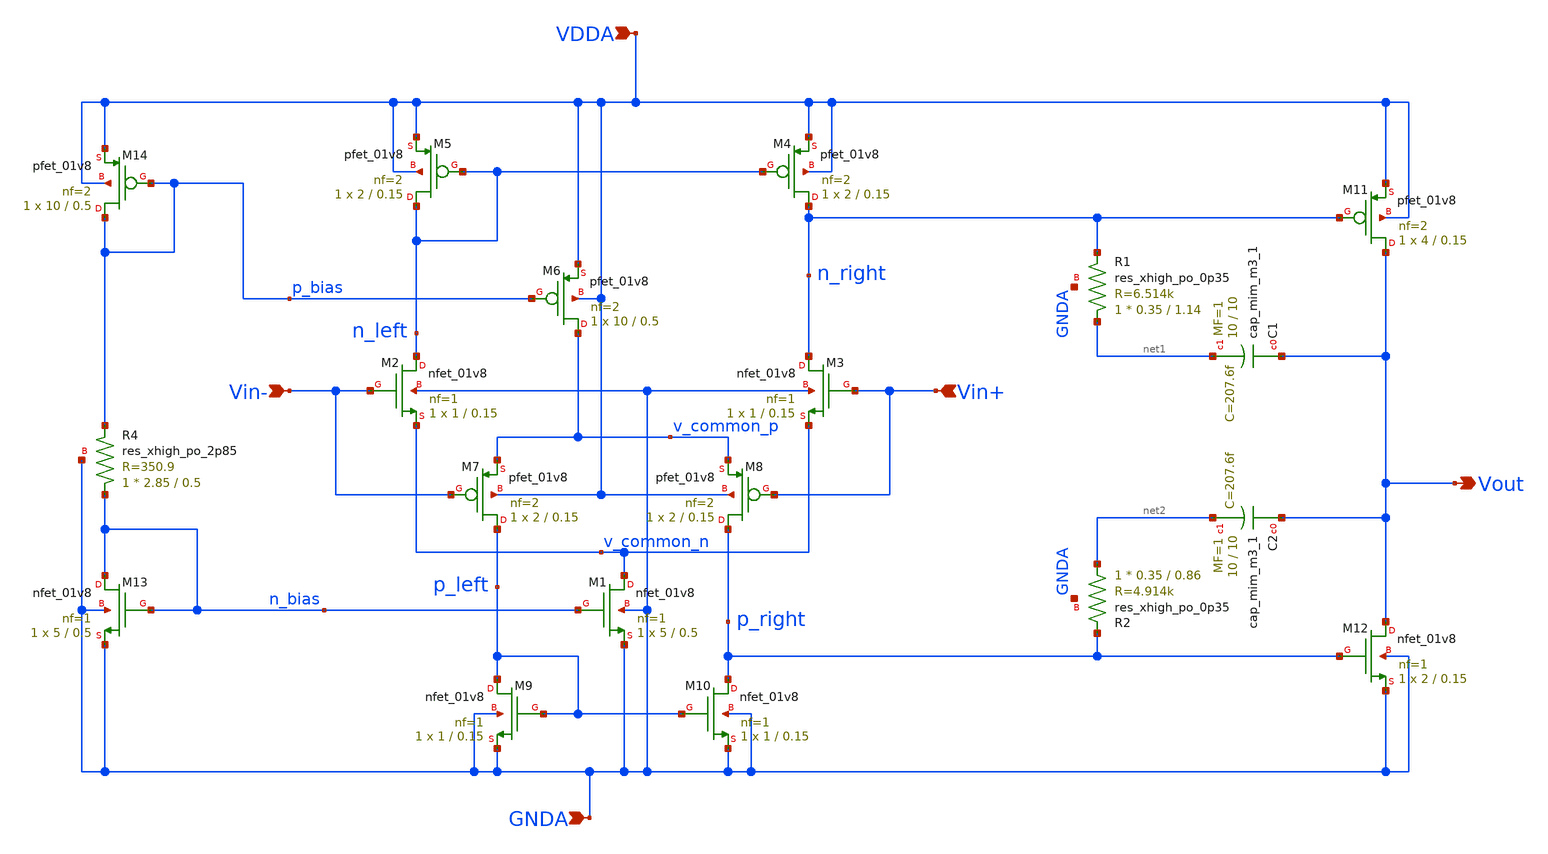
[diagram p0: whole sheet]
** sch_path: projects/pll/charge_pump/xschem_ngspice/rail_to_rail_opamp6_2.sch
**.subckt rail_to_rail_opamp6_2 Vout Vin+ Vin- VDDA GNDA
*.opin Vout
*.ipin Vin+
*.ipin Vin-
*.ipin VDDA
*.ipin GNDA
XM2 n_left Vin- v_common_n GNDA sky130_fd_pr__nfet_01v8 L=0.15 W=1 nf=1 ad='int((nf+1)/2) * W/nf * 0.29'
+ as='int((nf+2)/2) * W/nf * 0.29' pd='2*int((nf+1)/2) * (W/nf + 0.29)' ps='2*int((nf+2)/2) * (W/nf + 0.29)'
+ nrd='0.29 / W' nrs='0.29 / W' sa=0 sb=0 sd=0 mult=1 m=1
XM3 n_right Vin+ v_common_n GNDA sky130_fd_pr__nfet_01v8 L=0.15 W=1 nf=1 ad='int((nf+1)/2) * W/nf * 0.29'
+ as='int((nf+2)/2) * W/nf * 0.29' pd='2*int((nf+1)/2) * (W/nf + 0.29)' ps='2*int((nf+2)/2) * (W/nf + 0.29)'
+ nrd='0.29 / W' nrs='0.29 / W' sa=0 sb=0 sd=0 mult=1 m=1
XM5 n_left n_left VDDA VDDA sky130_fd_pr__pfet_01v8 L=0.15 W=2 nf=2 ad='int((nf+1)/2) * W/nf * 0.29'
+ as='int((nf+2)/2) * W/nf * 0.29' pd='2*int((nf+1)/2) * (W/nf + 0.29)' ps='2*int((nf+2)/2) * (W/nf + 0.29)'
+ nrd='0.29 / W' nrs='0.29 / W' sa=0 sb=0 sd=0 mult=1 m=1
XM4 n_right n_left VDDA VDDA sky130_fd_pr__pfet_01v8 L=0.15 W=2 nf=2 ad='int((nf+1)/2) * W/nf * 0.29'
+ as='int((nf+2)/2) * W/nf * 0.29' pd='2*int((nf+1)/2) * (W/nf + 0.29)' ps='2*int((nf+2)/2) * (W/nf + 0.29)'
+ nrd='0.29 / W' nrs='0.29 / W' sa=0 sb=0 sd=0 mult=1 m=1
XM6 v_common_p p_bias VDDA VDDA sky130_fd_pr__pfet_01v8 L=0.5 W=10 nf=2 ad='int((nf+1)/2) * W/nf * 0.29'
+ as='int((nf+2)/2) * W/nf * 0.29' pd='2*int((nf+1)/2) * (W/nf + 0.29)' ps='2*int((nf+2)/2) * (W/nf + 0.29)'
+ nrd='0.29 / W' nrs='0.29 / W' sa=0 sb=0 sd=0 mult=1 m=1
XM7 p_left Vin- v_common_p VDDA sky130_fd_pr__pfet_01v8 L=0.15 W=2 nf=2 ad='int((nf+1)/2) * W/nf * 0.29'
+ as='int((nf+2)/2) * W/nf * 0.29' pd='2*int((nf+1)/2) * (W/nf + 0.29)' ps='2*int((nf+2)/2) * (W/nf + 0.29)'
+ nrd='0.29 / W' nrs='0.29 / W' sa=0 sb=0 sd=0 mult=1 m=1
XM8 p_right Vin+ v_common_p VDDA sky130_fd_pr__pfet_01v8 L=0.15 W=2 nf=2 ad='int((nf+1)/2) * W/nf * 0.29'
+ as='int((nf+2)/2) * W/nf * 0.29' pd='2*int((nf+1)/2) * (W/nf + 0.29)' ps='2*int((nf+2)/2) * (W/nf + 0.29)'
+ nrd='0.29 / W' nrs='0.29 / W' sa=0 sb=0 sd=0 mult=1 m=1
XM9 p_left p_left GNDA GNDA sky130_fd_pr__nfet_01v8 L=0.15 W=1 nf=1 ad='int((nf+1)/2) * W/nf * 0.29'
+ as='int((nf+2)/2) * W/nf * 0.29' pd='2*int((nf+1)/2) * (W/nf + 0.29)' ps='2*int((nf+2)/2) * (W/nf + 0.29)'
+ nrd='0.29 / W' nrs='0.29 / W' sa=0 sb=0 sd=0 mult=1 m=1
XM10 p_right p_left GNDA GNDA sky130_fd_pr__nfet_01v8 L=0.15 W=1 nf=1 ad='int((nf+1)/2) * W/nf * 0.29'
+ as='int((nf+2)/2) * W/nf * 0.29' pd='2*int((nf+1)/2) * (W/nf + 0.29)' ps='2*int((nf+2)/2) * (W/nf + 0.29)'
+ nrd='0.29 / W' nrs='0.29 / W' sa=0 sb=0 sd=0 mult=1 m=1
XM1 v_common_n n_bias GNDA GNDA sky130_fd_pr__nfet_01v8 L=0.5 W=5 nf=1 ad='int((nf+1)/2) * W/nf * 0.29'
+ as='int((nf+2)/2) * W/nf * 0.29' pd='2*int((nf+1)/2) * (W/nf + 0.29)' ps='2*int((nf+2)/2) * (W/nf + 0.29)'
+ nrd='0.29 / W' nrs='0.29 / W' sa=0 sb=0 sd=0 mult=1 m=1
XM11 Vout n_right VDDA VDDA sky130_fd_pr__pfet_01v8 L=0.15 W=4 nf=2 ad='int((nf+1)/2) * W/nf * 0.29'
+ as='int((nf+2)/2) * W/nf * 0.29' pd='2*int((nf+1)/2) * (W/nf + 0.29)' ps='2*int((nf+2)/2) * (W/nf + 0.29)'
+ nrd='0.29 / W' nrs='0.29 / W' sa=0 sb=0 sd=0 mult=1 m=1
XM12 Vout p_right GNDA GNDA sky130_fd_pr__nfet_01v8 L=0.15 W=2 nf=1 ad='int((nf+1)/2) * W/nf * 0.29'
+ as='int((nf+2)/2) * W/nf * 0.29' pd='2*int((nf+1)/2) * (W/nf + 0.29)' ps='2*int((nf+2)/2) * (W/nf + 0.29)'
+ nrd='0.29 / W' nrs='0.29 / W' sa=0 sb=0 sd=0 mult=1 m=1
XM13 n_bias n_bias GNDA GNDA sky130_fd_pr__nfet_01v8 L=0.5 W=5 nf=1 ad='int((nf+1)/2) * W/nf * 0.29'
+ as='int((nf+2)/2) * W/nf * 0.29' pd='2*int((nf+1)/2) * (W/nf + 0.29)' ps='2*int((nf+2)/2) * (W/nf + 0.29)'
+ nrd='0.29 / W' nrs='0.29 / W' sa=0 sb=0 sd=0 mult=1 m=1
XM14 p_bias p_bias VDDA VDDA sky130_fd_pr__pfet_01v8 L=0.5 W=10 nf=2 ad='int((nf+1)/2) * W/nf * 0.29'
+ as='int((nf+2)/2) * W/nf * 0.29' pd='2*int((nf+1)/2) * (W/nf + 0.29)' ps='2*int((nf+2)/2) * (W/nf + 0.29)'
+ nrd='0.29 / W' nrs='0.29 / W' sa=0 sb=0 sd=0 mult=1 m=1
XC1 Vout net1 sky130_fd_pr__cap_mim_m3_1 W=10 L=10 MF=1 m=1
XC2 Vout net2 sky130_fd_pr__cap_mim_m3_1 W=10 L=10 MF=1 m=1
XR1 net1 n_right GNDA sky130_fd_pr__res_xhigh_po_0p35 L=1.14 mult=1 m=1
XR2 net2 p_right GNDA sky130_fd_pr__res_xhigh_po_0p35 L=0.86 mult=1 m=1
XR4 n_bias p_bias GNDA sky130_fd_pr__res_xhigh_po_2p85 L=0.5 mult=1 m=1
**.ends
.end
